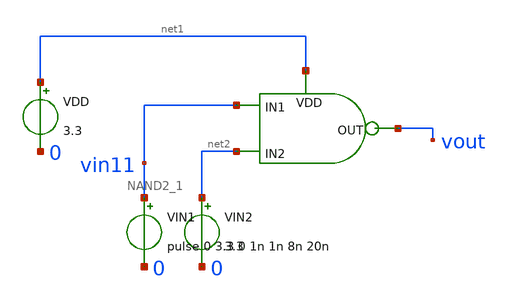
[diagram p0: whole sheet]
** sch_path: chipathon_2023/initial_notebooks_2023/accepted_notebooks/Current-Steering-DAC/DAC/Test_NAND2_1.sch
**.subckt Test_NAND2_1
VDD net1 0 3.3
VIN1 vin11 0 pulse 0 3.3 0 1n 1n 8n 20n
VIN2 net2 0 3.3
x1 net1 vin11 vout net2 NAND2_1
**** begin user architecture code




.include /foss/pdks/gf180mcuC/libs.tech/ngspice/design.ngspice
.lib /foss/pdks/gf180mcuC/libs.tech/ngspice/sm141064.ngspice typical


.control
	tran 0.1n 50n
	*dc vin1 0 3.3 0.1
	plot v(VIN11) V(vout)
	*plot v(vout)
.endc
.save all




**** end user architecture code
**.ends
.end
